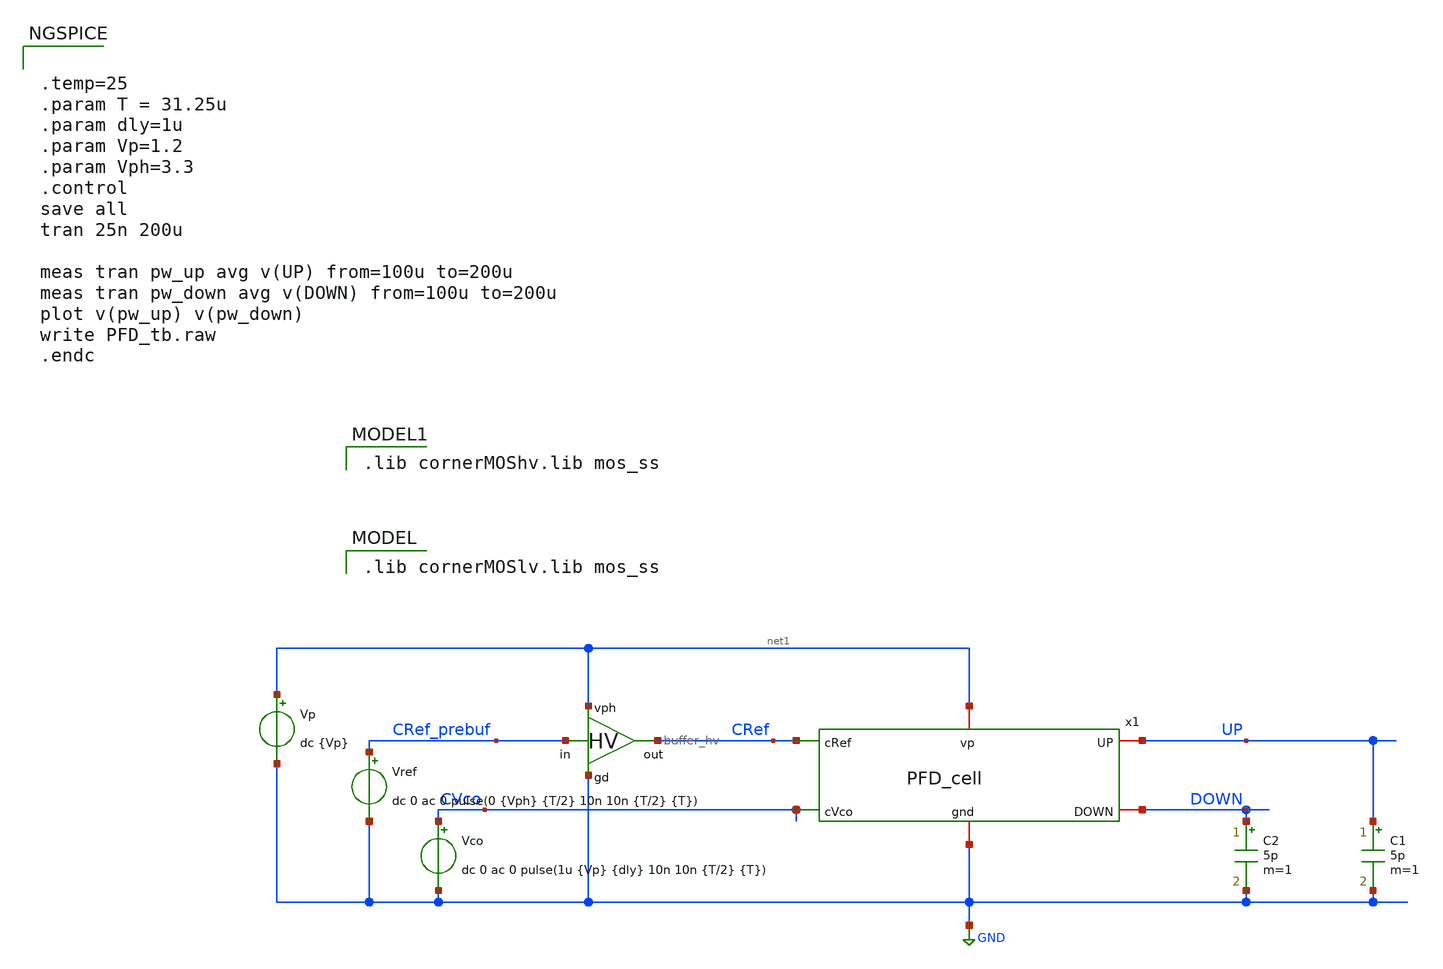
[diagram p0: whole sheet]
** sch_path: schematics/PFD/PFD_tb.sch
**.subckt PFD_tb
Vref CRef_prebuf GND dc 0 ac 0 pulse(0 {Vph} {T/2} 10n 10n {T/2} {T})
Vco CVco GND dc 0 ac 0 pulse(1u {Vp} {dly} 10n 10n {T/2} {T})
Vp net1 GND dc {Vp}
C1 UP GND 5p m=1
C2 DOWN GND 5p m=1
x1 GND net1 CRef UP DOWN CVco PFD_cell
x2 net1 CRef_prebuf CRef GND buffer_hv
**** begin user architecture code
 .lib cornerMOSlv.lib mos_ss



.temp=25
.param T = 31.25u
.param dly=1u
.param Vp=1.2
.param Vph=3.3
.control
save all
tran 25n 200u

meas tran pw_up avg v(UP) from=100u to=200u
meas tran pw_down avg v(DOWN) from=100u to=200u
plot v(pw_up) v(pw_down)
write PFD_tb.raw
.endc


 .lib cornerMOShv.lib mos_ss

**** end user architecture code
**.ends
.GLOBAL GND
.end
